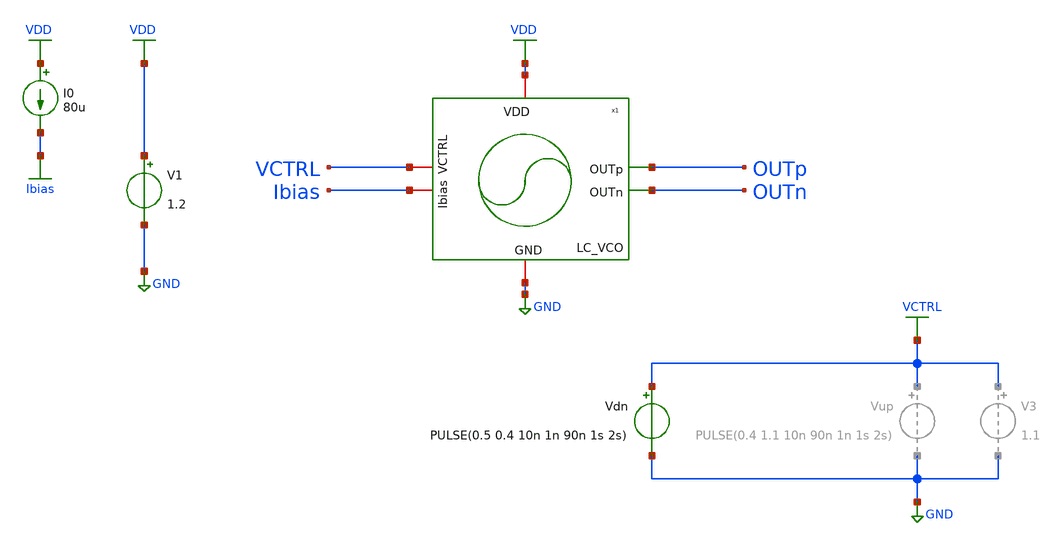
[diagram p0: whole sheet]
** sch_path: schematic/lc-vco/LC_VCO_tb.sch
**.subckt LC_VCO_tb
V1 VDD GND 1.2
I0 VDD Ibias 80u
x2 VDD OUTp OUTn Ibias VCTRL GND LC_VCO
Vdn VCTRL GND PULSE(0.5 0.4 10n 1n 90n 1s 2s)
**** begin user architecture code



.include ../ihp_4nh_inductor.spice
.param temp = 27
.options method=gear, rshunt=1.0e12

.control

* Save required signals
save v(OUTp) v(VCTRL)

* Long transient simulation
tran 10p 10.1u 100n

* Save raw waveform
write LC_VCO_tb.raw

* Plot transient waveform
let vout = v(OUTp)
plot vout v(Vctrl)

* Plot steady-state waveform
plot vout xlimit 200n 205n

* FFT analysis
setplot tran1
linearize vout
set specwindow=blackman
fft vout

* Plot FFT spectrum
let vout_db = db(vout)
plot vout_db xlimit 2.30G 2.50G ylimit -160 0

* Find the maximum magnitude value between 2G and 3G
meas sp max_vout_db max vout_db FROM=2G TO=3G

* Save FFT data
wrdata fft_output.txt frequency vout_db

* Save waveform for external processing
wrdata vco_waveform.txt vout_db

.endc




.lib cornerMOSlv.lib mos_tt
.lib cornerMOShv.lib mos_tt
.lib cornerRES.lib res_typ
.lib cornerCAP.lib cap_typ

**** end user architecture code
**.ends
.GLOBAL GND
.GLOBAL VDD
.GLOBAL Ibias
.GLOBAL VCTRL
.end
